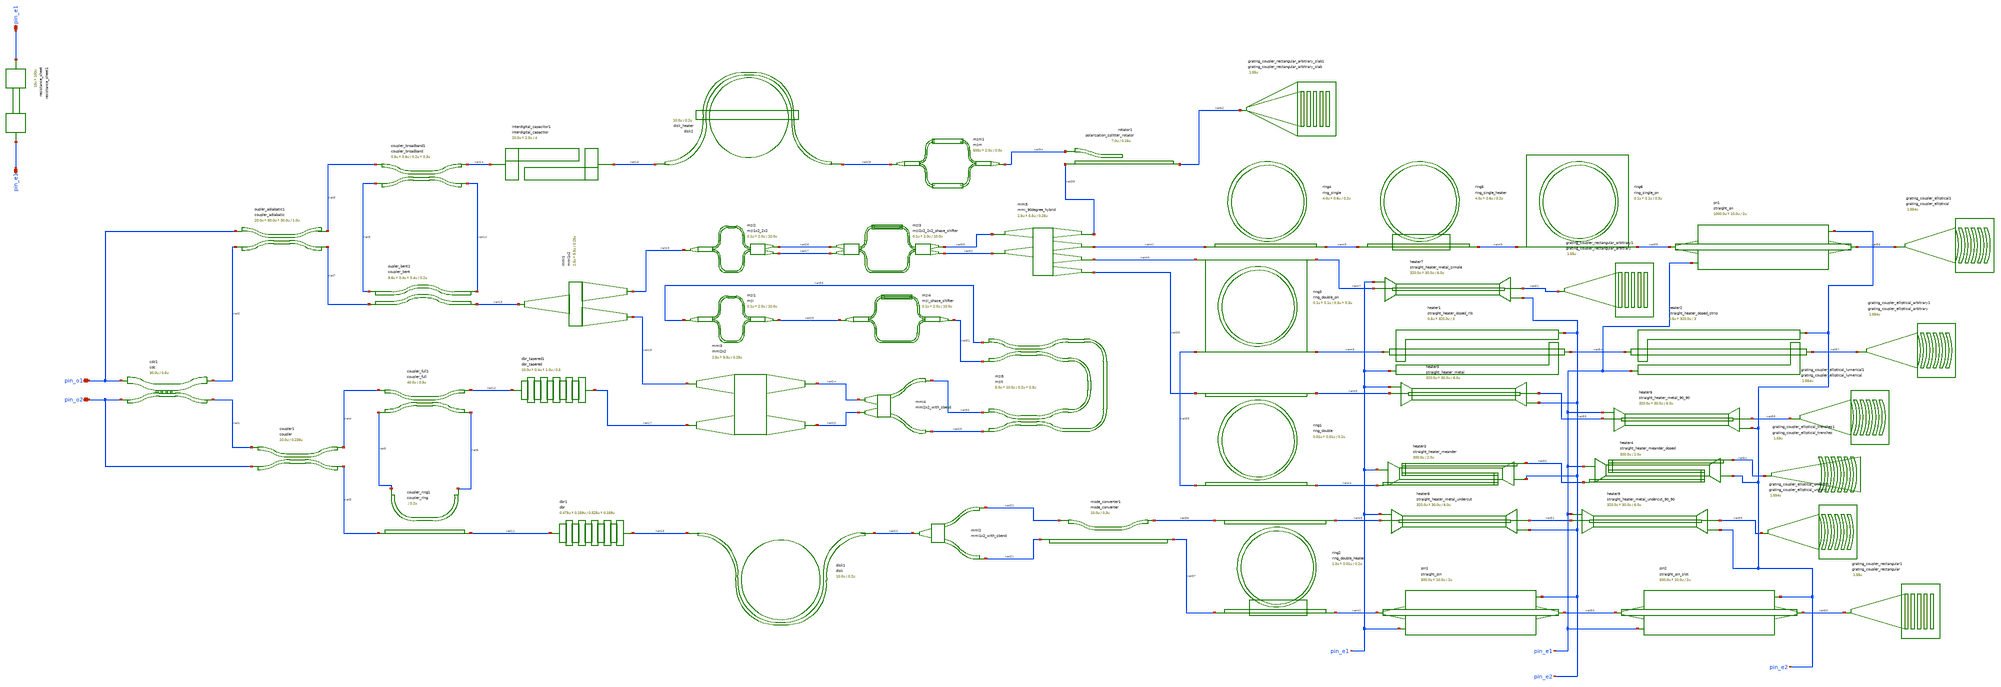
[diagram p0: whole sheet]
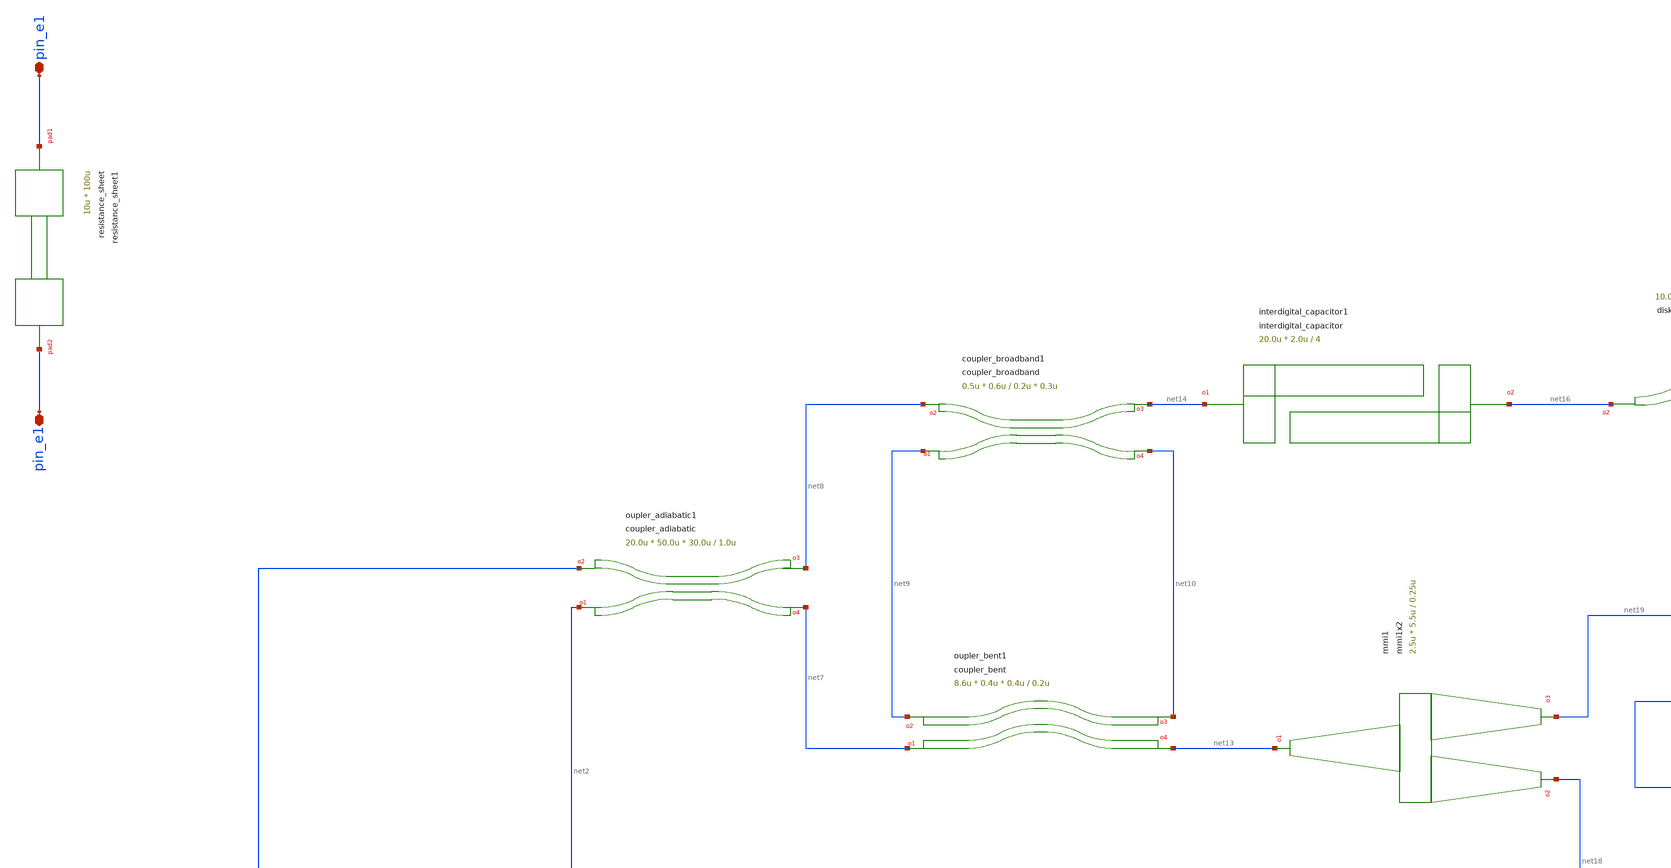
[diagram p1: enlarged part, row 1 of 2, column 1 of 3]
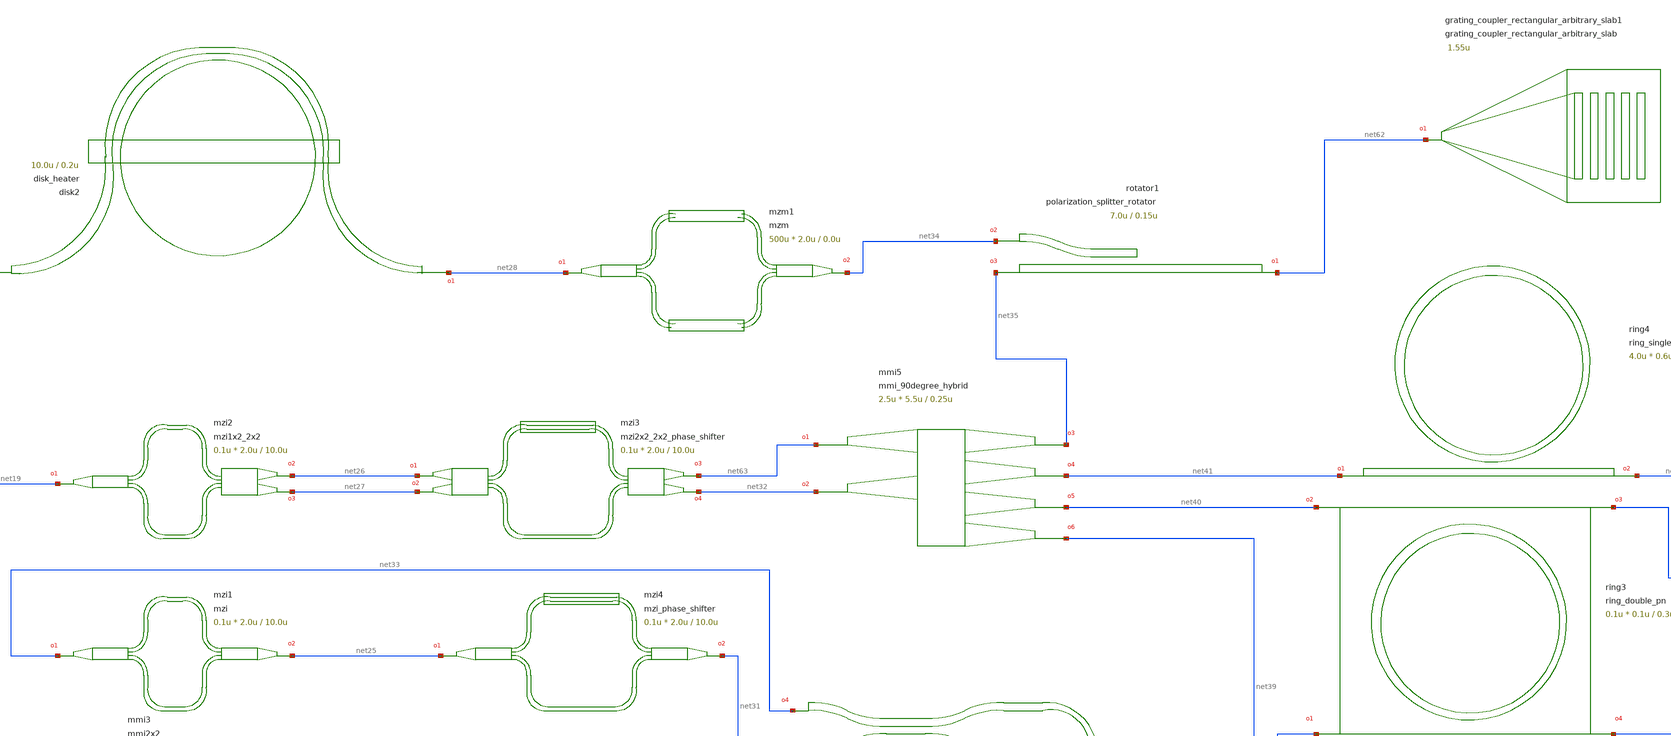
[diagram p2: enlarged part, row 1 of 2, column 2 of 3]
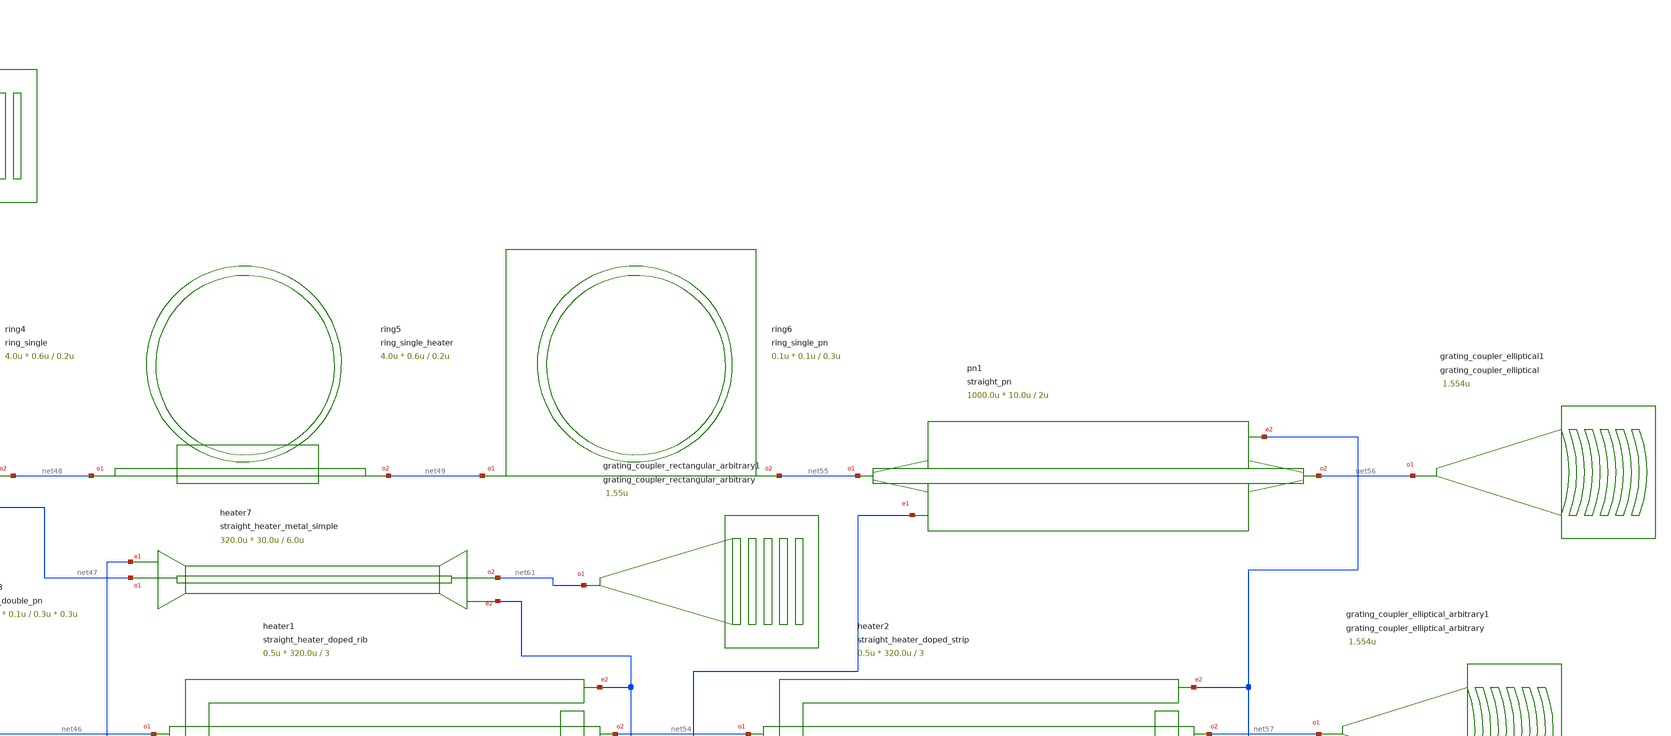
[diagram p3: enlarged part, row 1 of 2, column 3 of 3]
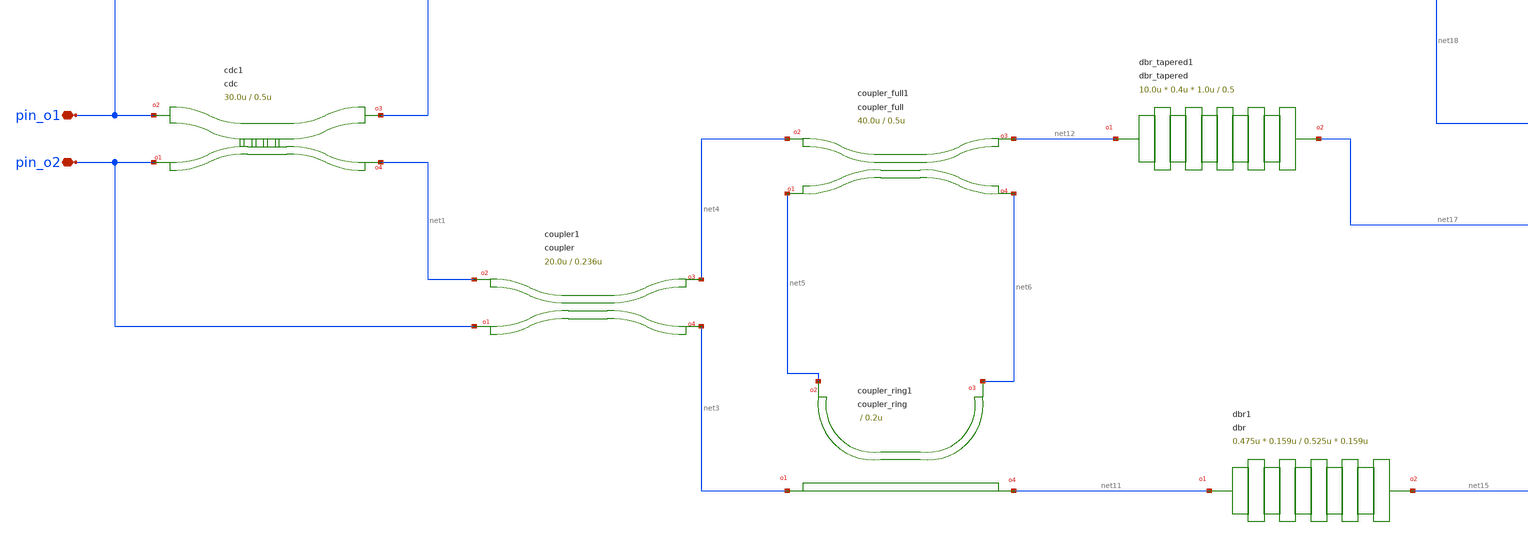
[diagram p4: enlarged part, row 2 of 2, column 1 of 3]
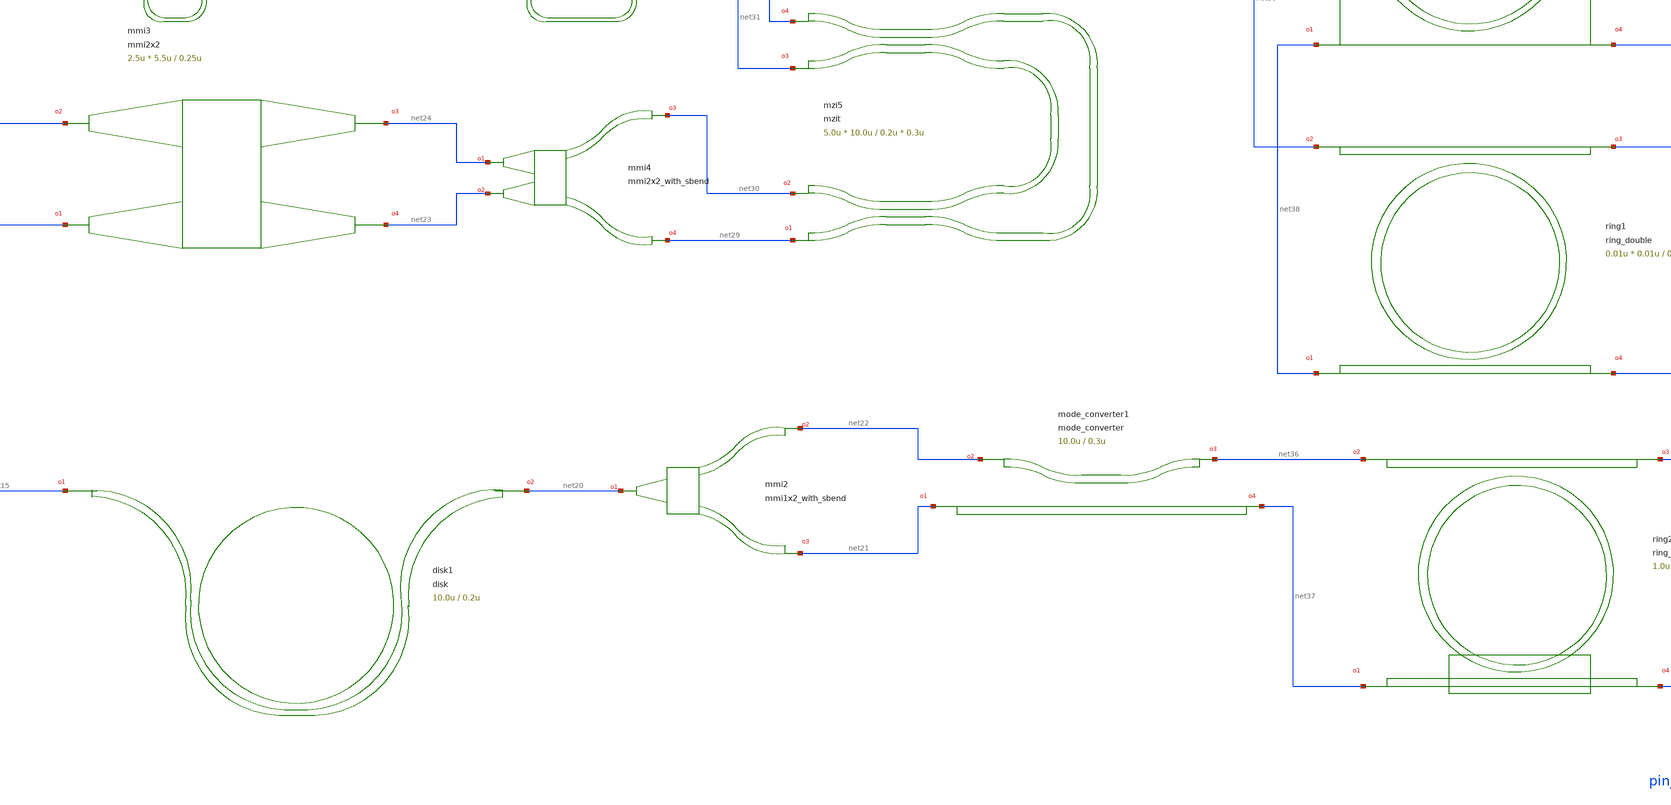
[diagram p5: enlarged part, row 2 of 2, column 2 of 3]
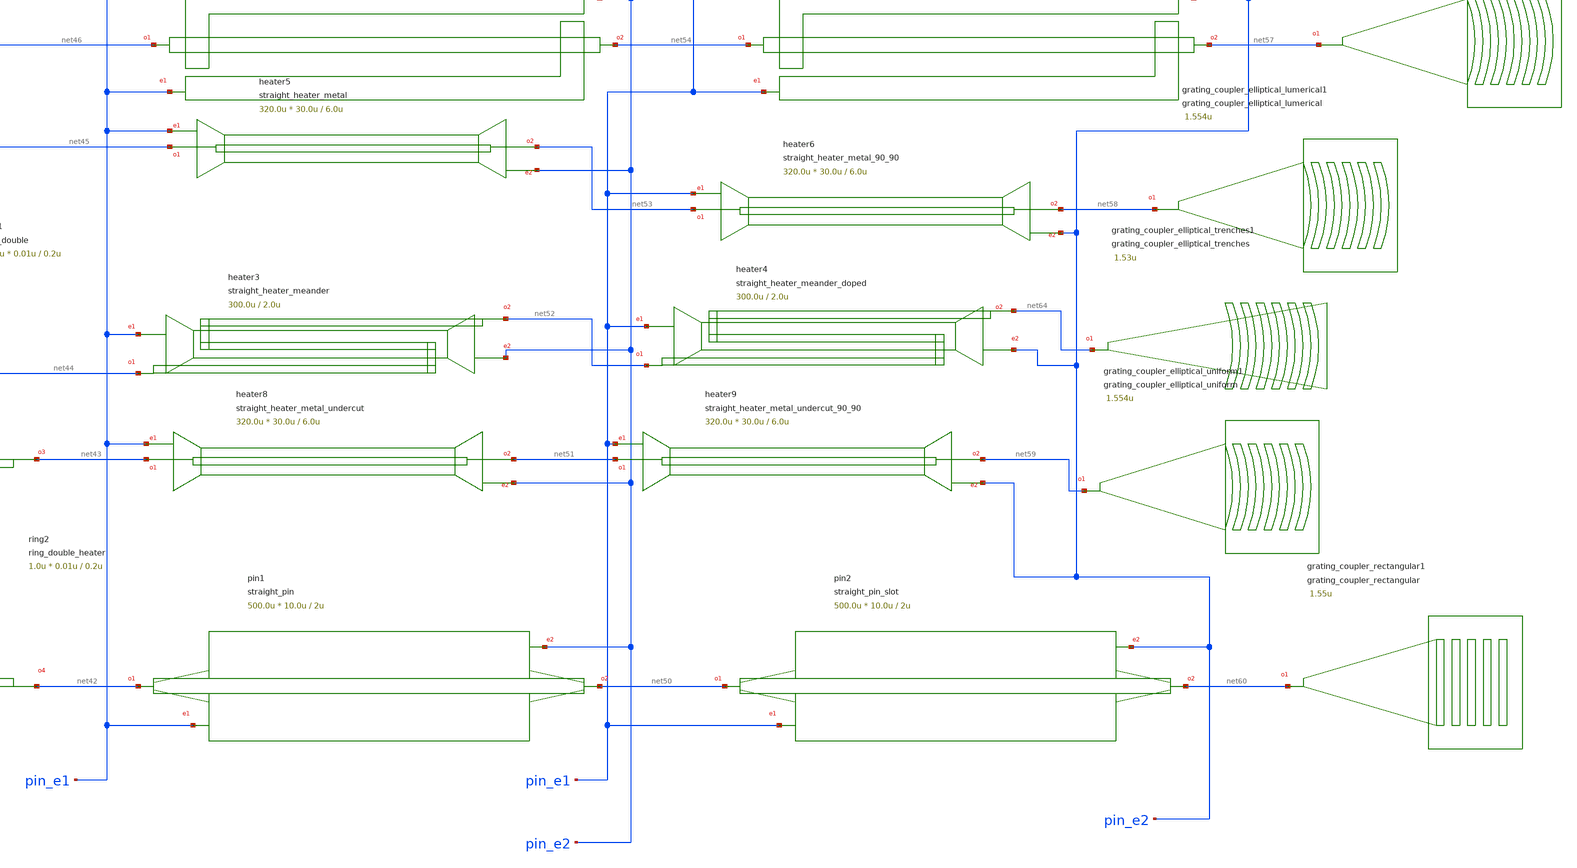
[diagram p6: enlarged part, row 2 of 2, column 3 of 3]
** sch_path: xschem/tests/test_sch/test_general3.sch
* Copyright (c) 2024, Mabrains LLC
* Licensed under the GNU Lesser General Public License, Version 3.0 (the "License");
* you may not use this file except in compliance with the License.
* GNU Lesser General Public License
* Version 3, 29 June 2007
* This program is free software: you can redistribute it and/or modify
* it under the terms of the GNU Lesser General Public License as published
* by the Free Software Foundation, either version 3 of the License, or
* (at your option) any later version.
* This program is distributed in the hope that it will be useful,
* but WITHOUT ANY WARRANTY; without even the implied warranty of
* MERCHANTABILITY or FITNESS FOR A PARTICULAR PURPOSE.  See the
* GNU Lesser General Public License for more details.
* You should have received a copy of the GNU Lesser General Public License
* along with this program.  If not, see <https://www.gnu.org/licenses/>.
* SPDX-License-Identifier: LGPL-3.0
**.subckt test_general3 pin_o2 pin_o1 pin_e1 pin_e1
*.iopin pin_o2
*.iopin pin_o1
*.iopin pin_e1
*.iopin pin_e1
Pcdc1 pin_o1 pin_o2 net2 net1 cdc length=30.0u gap=0.5u period=0.22 duty_cycle=0.5 width_top=2.0u
+ width_bot=0.75u dx=10u dy=1.8u
Pcoupler1 net1 pin_o2 net4 net3 coupler length=20.0u gap=0.236u dx=10u dy=4.0u
Poupler_adiabatic1 pin_o1 net2 net7 net8 coupler_adiabatic length1=20.0u length2=50.0u length3=30.0u
+ wg_sep=1.0u input_wg_sep=3.0u output_wg_sep=3.0u dw=0.1u
Poupler_bent1 net9 net7 net10 net13 coupler_bent gap=0.2u radius=26u length=8.6u width1=0.4u
+ width2=0.4u length_straight=10u
Pcoupler_broadband1 net8 net9 net14 net10 coupler_broadband w_sc=0.5u gap_sc=0.2u w_top=0.6u
+ gap_pc=0.3u length_taper=1.0u length_coupler_straight=12.4u length_coupler_big_gap=4.7u radius=10.0u
Pcoupler_full1 net4 net5 net12 net6 coupler_full coupling_length=40.0u dx=10.0u dy=4.8u gap=0.5u
+ dw=0.1u
Pcoupler_ring1 net3 net11 net6 net5 coupler_ring gap=0.2u radius=5.0u length_x=4.0u
+ length_extension=3.0u
Pdbr1 net11 net15 dbr w1=0.475u l1=0.159u w2=0.525u l2=0.159u n=10
Pdbr_tapered1 net12 net17 dbr_tapered length=10.0u period=0.85 duty_cycle=0.5 w1=0.4u w2=1.0u
+ taper_length=20.0u
Pdisk1 net15 net20 disk radius=10.0u gap=0.2u wrap_angle_deg=180.0 parity=1
Pdisk2 net28 net16 disk_heater radius=10.0u gap=0.2u wrap_angle_deg=180.0 parity=1 heater_width=5.0u
+ heater_extent=2.0u
Pinterdigital_capacitor1 net14 net16 interdigital_capacitor fingers=4 finger_length=20.0u
+ finger_gap=2.0u thickness=5.0u
Pmmi1 net13 net18 net19 mmi1x2 width=0.5u width_taper=1u length_taper=10u length_mmi=5.5u
+ width_mmi=2.5u gap_mmi=0.25u
Pmmi2 net20 net22 net21 mmi1x2_with_sbend
Pmmi3 net17 net18 net24 net23 mmi2x2 width=0.5u width_taper=1u length_taper=10u length_mmi=5.5u
+ width_mmi=2.5u gap_mmi=0.25u
Pmmi4 net24 net23 net30 net29 mmi2x2_with_sbend
Pmmi5 net63 net32 net35 net41 net40 net39 mmi_90degree_hybrid width=0.5u width_taper=1u
+ length_taper=10u length_mmi=5.5u width_mmi=2.5u gap_mmi=0.25u
Pmode_converter1 net21 net22 net36 net37 mode_converter gap=0.3u length=10.0u mm_width=1.2u
+ mc_mm_width=1.0u sm_width=0.5u
Pmzi1 net33 net25 mzi delta_length=10.0u length_y=2.0u length_x=0.1u
Pmzi2 net19 net26 net27 mzi1x2_2x2 delta_length=10.0u length_y=2.0u length_x=0.1u
Pmzi3 net26 net27 net63 net32 mzi2x2_2x2_phase_shifter delta_length=10.0u length_y=2.0u
+ length_x=0.1u
Pmzi4 net25 net31 mzi_phase_shifter delta_length=10.0u length_y=2.0u length_x=0.1u
Pmzi5 net29 net30 net31 net33 mzit w0=0.5u w1=0.45u w2=0.55u dy=2.0u delta_length=10.0u length=1.0u
+ coupler_length1=5.0u coupler_length2=10.0u coupler_gap1=0.2u coupler_gap2=0.3u taper_length=5.0u
Pmzm1 net28 net34 mzm length_x=500u length_y=2.0u delta_length=0.0u
Protator1 net62 net34 net35 polarization_splitter_rotator width_taper_in1=0.54u
+ width_taper_in2=0.69u width_taper_in3=0.83u length_taper_in1=4.0u length_taper_in2=44.0u length_taper_in3=44.0u
+ width_coupler_top=0.9u width_coupler_bottom=0.405u length_coupler=7.0u gap=0.15u width_out=0.54u length_out=14.33u dy=5.0u
Presistance_sheet1 pin_e1 pin_e1 resistance_sheet width=10u pad_pitch=100u
Pring1 net39 net38 net44 net45 ring_double gap=0.2u radius=10.0u length_x=0.01u length_y=0.01u
Pring2 net37 net36 net43 net42 ring_double_heater gap=0.2u gap_top=0.2u radius=10.0u length_x=1.0u
+ length_y=0.01u
Pring3 net40 net38 net46 net47 ring_double_pn add_gap=0.3u drop_gap=0.3u radius=5.0u doping_angle=85
+ length_x=0.1u length_y=0.1u
Pring4 net41 net48 ring_single gap=0.2u radius=10.0u length_x=4.0u length_y=0.6u
Pring5 net48 net49 ring_single_heater gap=0.2u radius=10.0u length_x=4.0u length_y=0.6u
Pring6 net49 net55 ring_single_pn gap=0.3u radius=5.0u doping_angle=250 length_x=0.1u length_y=0.1u
Pheater1 net46 net54 pin_e1 pin_e2 straight_heater_doped_rib length=320.0u nsections=3
+ heater_width=2.0u heater_gap=0.8u via_stack_gap=0.0u width=0.5u xoffset_tip1=0.2u xoffset_tip2=0.4u
Pheater2 net54 net57 pin_e1 pin_e2 straight_heater_doped_strip length=320.0u nsections=3
+ heater_width=2.0u heater_gap=0.8u via_stack_gap=0.0u width=0.5u xoffset_tip1=0.2u xoffset_tip2=0.4u
Pheater3 net44 net52 pin_e1 pin_e2 straight_heater_meander length=300.0u spacing=2.0u
+ heater_width=2.5u extension_length=15.0u radius=90u heater_taper_length=10.0u taper_length=10.0u
Pheater4 net52 net64 pin_e1 pin_e2 straight_heater_meander_doped length=300.0u spacing=2.0u
+ heater_width=1.5u extension_length=15.0u radius=90u taper_length=10.0u
Pheater5 net45 net53 pin_e1 pin_e2 straight_heater_metal length=320.0u length_undercut_spacing=6.0u
+ length_undercut=30.0u length_straight_input=15.0u heater_taper_length=5.0u
Pheater6 net53 net58 pin_e1 pin_e2 straight_heater_metal_90_90 length=320.0u
+ length_undercut_spacing=6.0u length_undercut=30.0u length_straight_input=15.0u heater_taper_length=5.0u
Pheater7 net47 net61 pin_e1 pin_e2 straight_heater_metal_simple length=320.0u
+ length_undercut_spacing=6.0u length_undercut=30.0u heater_taper_length=5.0u
Pheater8 net43 net51 pin_e1 pin_e2 straight_heater_metal_undercut length=320.0u
+ length_undercut_spacing=6.0u length_undercut=30.0u length_straight_input=15.0u heater_taper_length=5.0u
Pheater9 net51 net59 pin_e1 pin_e2 straight_heater_metal_undercut_90_90 length=320.0u
+ length_undercut_spacing=6.0u length_undercut=30.0u length_straight_input=15.0u heater_taper_length=5.0u
Ppin1 net42 net50 pin_e1 pin_e2 straight_pin length=500.0u via_stack_width=10.0u
+ via_stack_spacing=2u
Ppin2 net50 net60 pin_e1 pin_e2 straight_pin_slot length=500.0u via_stack_width=10.0u
+ via_stack_slab_width=10.0u via_stack_spacing=2u via_stack_slab_spacing=2.0u
Ppn1 net55 net56 pin_e1 pin_e2 straight_pn length=1000.0u via_stack_width=10.0u via_stack_spacing=2u
Pgrating_coupler_elliptical1 net56 grating_coupler_elliptical taper_length=16.6u taper_angle=40.0
+ wavelength=1.554u fiber_angle=15.0 grating_line_width=0.343u n_periods=30 slab_xmin=-1.0u slab_offset=2.0u
Pgrating_coupler_elliptical_arbitrary1 net57 grating_coupler_elliptical_arbitrary
+ gaps=[0.1,0.1,0.1,0.1,0.1,0.1,0.1,0.1,0.1,0.1] widths=[0.5,0.5,0.5,0.5,0.5,0.5,0.5,0.5,0.5,0.5] taper_length=16.6u taper_angle=60.0
+ wavelength=1.554u fiber_angle=15.0 taper_to_slab_offset=-3.0u
Pgrating_coupler_elliptical_lumerical1 net58 grating_coupler_elliptical_lumerical
+ parameters=[-2.43u, taper_angle=55.0 taper_length=12.6u fiber_angle=5.0 bias_gap=0.0u wavelength=1.554u
Pgrating_coupler_elliptical_trenches1 net64 grating_coupler_elliptical_trenches taper_length=16.6u
+ taper_angle=30.0 wavelength=1.53u fiber_angle=15.0 grating_line_width=0.343u p_start=26 n_periods=30
+ end_straight_length=0.2u
Pgrating_coupler_elliptical_uniform1 net59 grating_coupler_elliptical_uniform n_periods=20
+ period=0.75 fill_factor=0.5 taper_length=16.6u taper_angle=60.0 wavelength=1.554u fiber_angle=15.0
+ taper_to_slab_offset=-3.0u bias_gap=0.0u
Pgrating_coupler_rectangular1 net60 grating_coupler_rectangular n_periods=20 period=0.75
+ fill_factor=0.5 width_grating=11.0u length_taper=150.0u wavelength=1.55u fiber_angle=15 slab_xmin=-1.0u
+ slab_offset=1.0u
Pgrating_coupler_rectangular_arbitrary1 net61 grating_coupler_rectangular_arbitrary gaps=[0.2u,
+ widths=[0.5,0.5,0.5,0.5,0.5,0.5,0.5,0.5,0.5,0.5] width_grating=11.0u length_taper=150.0u wavelength=1.55u slab_xmin=-1.0u slab_offset=1.0u
+ fiber_angle=15
Pgrating_coupler_rectangular_arbitrary_slab1 net62 grating_coupler_rectangular_arbitrary_slab
+ gaps=[0.2u, widths=[0.5,0.5,0.5,0.5,0.5,0.5,0.5,0.5,0.5,0.5] width_grating=11.0u length_taper=150.0u
+ wavelength=1.55u slab_offset=2.0u fiber_angle=15
**.ends
.end
